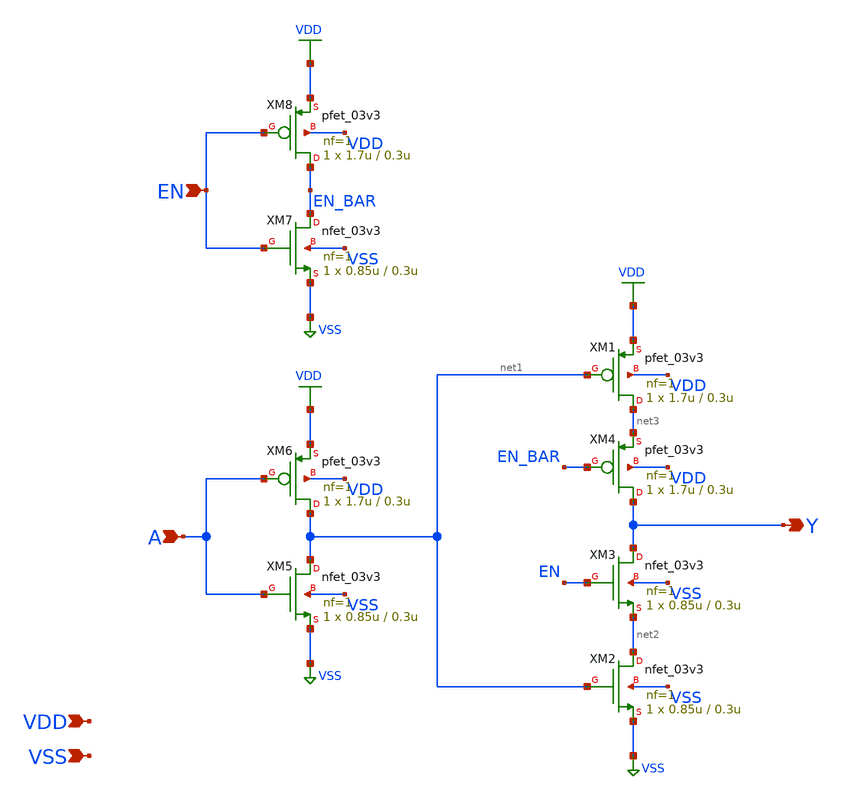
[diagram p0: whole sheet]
** sch_path: gf180mcu_osu_sc_gp9t3v3/xschem/gf180mcu_osu_sc_gp9t3v3__tbuf_1.sch
**.subckt gf180mcu_osu_sc_gp9t3v3__tbuf_1 A EN Y VDD VSS
*.ipin A
*.ipin EN
*.opin Y
*.ipin VDD
*.ipin VSS
XM1 net3 net1 VDD VDD pfet_03v3 L=0.3u W=1.7u nf=1 ad='int((nf+1)/2) * W/nf * 0.18u' as='int((nf+2)/2) * W/nf * 0.18u'
+ pd='2*int((nf+1)/2) * (W/nf + 0.18u)' ps='2*int((nf+2)/2) * (W/nf + 0.18u)' nrd='0.18u / W' nrs='0.18u / W'
+ sa=0 sb=0 sd=0 m=1
XM2 net2 net1 VSS VSS nfet_03v3 L=0.3u W=0.85u nf=1 ad='int((nf+1)/2) * W/nf * 0.18u' as='int((nf+2)/2) * W/nf * 0.18u'
+ pd='2*int((nf+1)/2) * (W/nf + 0.18u)' ps='2*int((nf+2)/2) * (W/nf + 0.18u)' nrd='0.18u / W' nrs='0.18u / W'
+ sa=0 sb=0 sd=0 m=1
XM3 Y EN net2 VSS nfet_03v3 L=0.3u W=0.85u nf=1 ad='int((nf+1)/2) * W/nf * 0.18u' as='int((nf+2)/2) * W/nf * 0.18u'
+ pd='2*int((nf+1)/2) * (W/nf + 0.18u)' ps='2*int((nf+2)/2) * (W/nf + 0.18u)' nrd='0.18u / W' nrs='0.18u / W'
+ sa=0 sb=0 sd=0 m=1
XM4 Y EN_BAR net3 VDD pfet_03v3 L=0.3u W=1.7u nf=1 ad='int((nf+1)/2) * W/nf * 0.18u' as='int((nf+2)/2) * W/nf * 0.18u'
+ pd='2*int((nf+1)/2) * (W/nf + 0.18u)' ps='2*int((nf+2)/2) * (W/nf + 0.18u)' nrd='0.18u / W' nrs='0.18u / W'
+ sa=0 sb=0 sd=0 m=1
XM5 net1 A VSS VSS nfet_03v3 L=0.3u W=0.85u nf=1 ad='int((nf+1)/2) * W/nf * 0.18u' as='int((nf+2)/2) * W/nf * 0.18u'
+ pd='2*int((nf+1)/2) * (W/nf + 0.18u)' ps='2*int((nf+2)/2) * (W/nf + 0.18u)' nrd='0.18u / W' nrs='0.18u / W'
+ sa=0 sb=0 sd=0 m=1
XM6 net1 A VDD VDD pfet_03v3 L=0.3u W=1.7u nf=1 ad='int((nf+1)/2) * W/nf * 0.18u' as='int((nf+2)/2) * W/nf * 0.18u'
+ pd='2*int((nf+1)/2) * (W/nf + 0.18u)' ps='2*int((nf+2)/2) * (W/nf + 0.18u)' nrd='0.18u / W' nrs='0.18u / W'
+ sa=0 sb=0 sd=0 m=1
XM7 EN_BAR EN VSS VSS nfet_03v3 L=0.3u W=0.85u nf=1 ad='int((nf+1)/2) * W/nf * 0.18u' as='int((nf+2)/2) * W/nf * 0.18u'
+ pd='2*int((nf+1)/2) * (W/nf + 0.18u)' ps='2*int((nf+2)/2) * (W/nf + 0.18u)' nrd='0.18u / W' nrs='0.18u / W'
+ sa=0 sb=0 sd=0 m=1
XM8 EN_BAR EN VDD VDD pfet_03v3 L=0.3u W=1.7u nf=1 ad='int((nf+1)/2) * W/nf * 0.18u' as='int((nf+2)/2) * W/nf * 0.18u'
+ pd='2*int((nf+1)/2) * (W/nf + 0.18u)' ps='2*int((nf+2)/2) * (W/nf + 0.18u)' nrd='0.18u / W' nrs='0.18u / W'
+ sa=0 sb=0 sd=0 m=1
**.ends
.GLOBAL VDD
.GLOBAL VSS
.end
